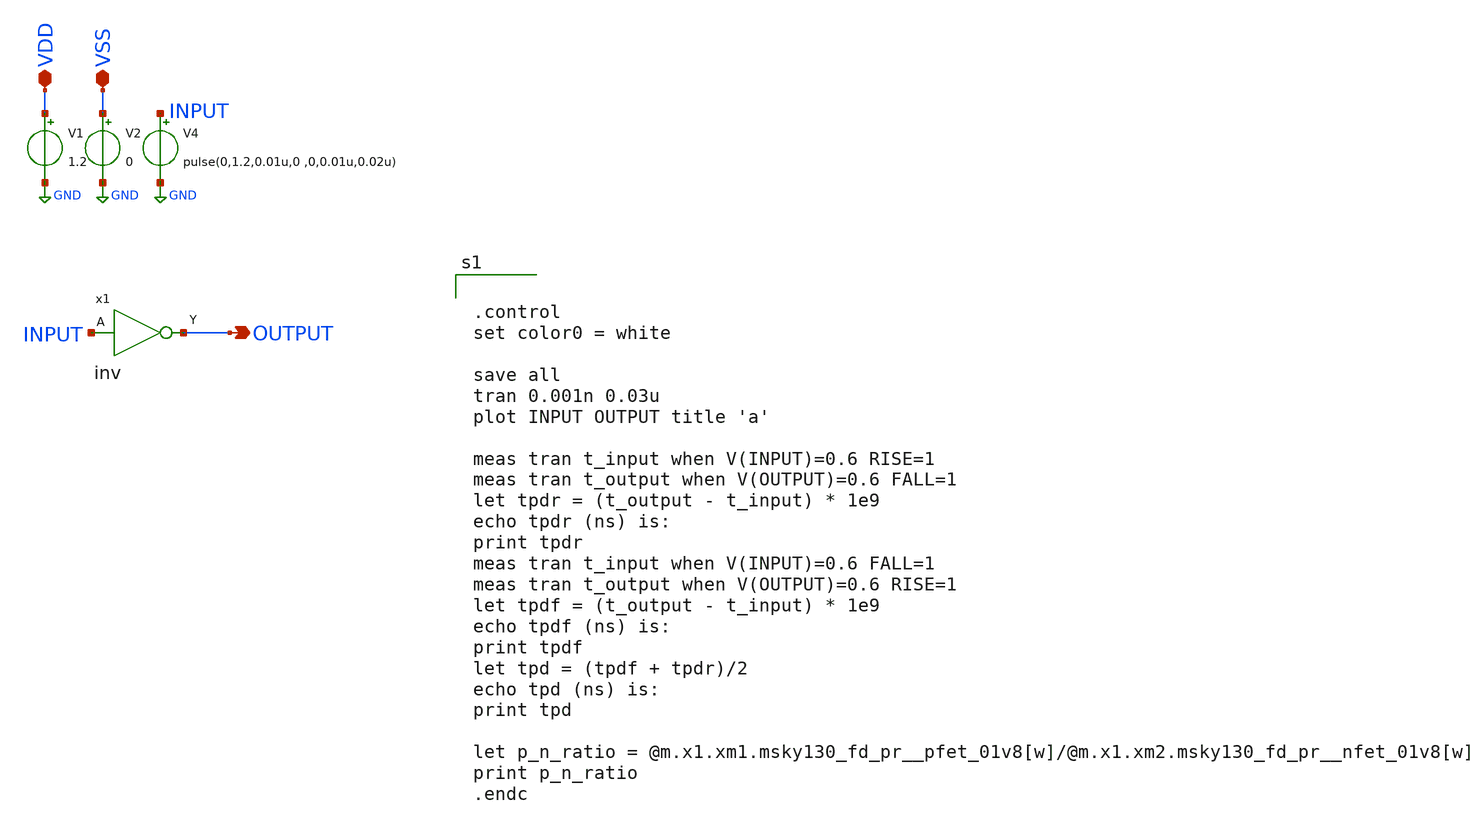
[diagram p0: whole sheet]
** sch_path: design/xschem/INV/inv_TB.sch
**.subckt inv_TB OUTPUT VSS VDD
*.opin OUTPUT
*.iopin VSS
*.iopin VDD
V1 VDD GND 1.2
V2 VSS GND 0
V4 INPUT GND pulse(0,1.2,0.01u,0 ,0,0.01u,0.02u)
x1 INPUT VSS VDD OUTPUT inv
**** begin user architecture code

** opencircuitdesign pdks install
.lib $::SKYWATER_MODELS/sky130.lib.spice tt_mm




.control
set color0 = white

save all
tran 0.001n 0.03u
plot INPUT OUTPUT title 'a'

meas tran t_input when V(INPUT)=0.6 RISE=1
meas tran t_output when V(OUTPUT)=0.6 FALL=1
let tpdr = (t_output - t_input) * 1e9
echo tpdr (ns) is:
print tpdr
meas tran t_input when V(INPUT)=0.6 FALL=1
meas tran t_output when V(OUTPUT)=0.6 RISE=1
let tpdf = (t_output - t_input) * 1e9
echo tpdf (ns) is:
print tpdf
let tpd = (tpdf + tpdr)/2
echo tpd (ns) is:
print tpd

let p_n_ratio = @m.x1.xm1.msky130_fd_pr__pfet_01v8[w]/@m.x1.xm2.msky130_fd_pr__nfet_01v8[w]
print p_n_ratio
.endc


**** end user architecture code
**.ends

* expanding   symbol:  INV/inv.sym # of pins=2
** sym_path: design/xschem/INV/inv.sym
** sch_path: design/xschem/INV/inv.sch
.subckt inv A VSS VDD Y
*.ipin A
*.opin Y
XM1 Y A VDD VDD sky130_fd_pr__pfet_01v8 L=0.15 W=3.2 nf=1 ad='int((nf+1)/2) * W/nf * 0.29' as='int((nf+2)/2) * W/nf * 0.29'
+ pd='2*int((nf+1)/2) * (W/nf + 0.29)' ps='2*int((nf+2)/2) * (W/nf + 0.29)' nrd='0.29 / W' nrs='0.29 / W'
+ sa=0 sb=0 sd=0 mult=1 m=1
XM2 Y A VSS VSS sky130_fd_pr__nfet_01v8 L=0.15 W=1 nf=1 ad='int((nf+1)/2) * W/nf * 0.29' as='int((nf+2)/2) * W/nf * 0.29'
+ pd='2*int((nf+1)/2) * (W/nf + 0.29)' ps='2*int((nf+2)/2) * (W/nf + 0.29)' nrd='0.29 / W' nrs='0.29 / W'
+ sa=0 sb=0 sd=0 mult=1 m=1
.ends

.GLOBAL GND
.end
